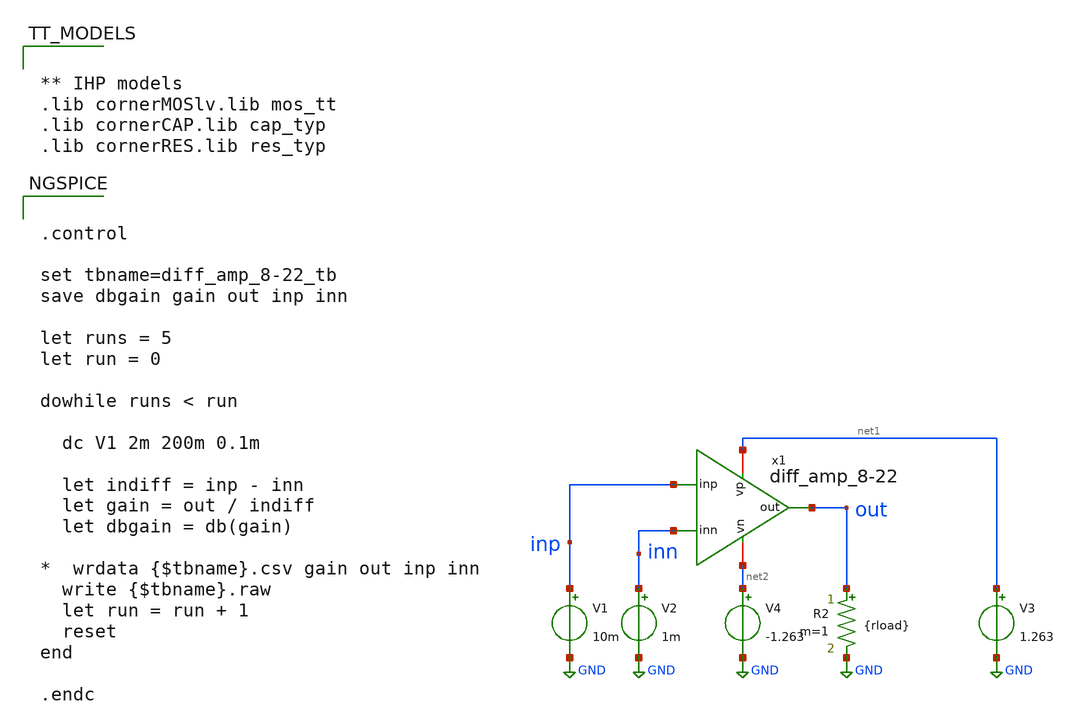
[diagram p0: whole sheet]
** sch_path: TempSensor/design_data/xschem/diff_amp_8-22_tb.sch
**.subckt diff_amp_8-22_tb
V2 inn GND 1m
V1 inp GND 10m
V3 net1 GND 1.263
V4 net2 GND -1.263
x1 net1 out inp inn net2 diff_amp_8-22
R2 out GND {rload} m=1
**** begin user architecture code


** IHP models
.lib cornerMOSlv.lib mos_tt
.lib cornerCAP.lib cap_typ
.lib cornerRES.lib res_typ




.control

set tbname=diff_amp_8-22_tb
save dbgain gain out inp inn

let runs = 5
let run = 0

dowhile runs < run

  dc V1 2m 200m 0.1m

  let indiff = inp - inn
  let gain = out / indiff
  let dbgain = db(gain)

*  wrdata {$tbname}.csv gain out inp inn
  write {$tbname}.raw
  let run = run + 1
  reset
end

.endc


**** end user architecture code
**.ends

* expanding   symbol:  practicing/TempSensor/design_data/xschem/diff_amp_8-22.sym # of pins=5
** sym_path: TempSensor/design_data/xschem/diff_amp_8-22.sym
** sch_path: TempSensor/design_data/xschem/diff_amp_8-22.sch
.subckt diff_amp_8-22 vp out inp inn vn
*.opin out
*.iopin vn
*.iopin vp
*.ipin inp
*.ipin inn
XM5 net18 net1 vp vp sg13_lv_pmos w=10u l=3.33u ng=1 m=1 mm_ok=1
XM30 net15 inn net6 vn sg13_lv_nmos w=10u l=1.5u ng=1 m=5 mm_ok=1
I0 vp net4 5u
XM7 net19 net1 vp vp sg13_lv_pmos w=10u l=3.33u ng=1 m=2 mm_ok=1
XM6 net1 net1 net18 vp sg13_lv_pmos w=10u l=1u ng=1 m=1 mm_ok=1
XM8 net5 net1 net19 vp sg13_lv_pmos w=10u l=.5u ng=1 m=1 mm_ok=1
XM11 net15 net7 vp vp sg13_lv_pmos w=10u l=2.5u ng=1 m=5 mm_ok=1
XM13 net16 net7 vp vp sg13_lv_pmos w=10u l=2.5u ng=1 m=5 mm_ok=1
XM12 net7 net7 net15 vp sg13_lv_pmos w=10u l=1u ng=1 m=5 mm_ok=1
XM14 out net7 net16 vp sg13_lv_pmos w=10u l=1u ng=1 m=5 mm_ok=1
XM21 net12 net12 vp vp sg13_lv_pmos w=10u l=.33u ng=1 m=10 mm_ok=1
XM24 net13 net1 vp vp sg13_lv_pmos w=4u l=5u ng=1 m=1 mm_ok=1
XM22 net11 net11 net12 vp sg13_lv_pmos w=10u l=.33u ng=1 m=10 mm_ok=1
XM29 vp inp net6 vn sg13_lv_nmos w=10u l=1.5u ng=1 m=5 mm_ok=1
XM9 net9 inp net5 net5 sg13_lv_pmos w=10u l=1.5u ng=1 m=10 mm_ok=1
XM10 net8 inn net5 net5 sg13_lv_pmos w=10u l=1.5u ng=1 m=10 mm_ok=1
XM1 net4 net4 net3 vn sg13_lv_nmos w=10u l=2u ng=1 m=1 mm_ok=1
XM2 net3 net4 vn vn sg13_lv_nmos w=5u l=5u ng=1 m=1 mm_ok=1
XM3 net1 net4 net2 vn sg13_lv_nmos w=10u l=2u ng=1 m=1 mm_ok=1
XM4 net2 net4 vn vn sg13_lv_nmos w=5u l=5u ng=1 m=1 mm_ok=1
XM31 net6 net4 net17 vn sg13_lv_nmos w=10u l=1u ng=1 m=1 mm_ok=1
XM32 net17 net4 vn vn sg13_lv_nmos w=10u l=5u ng=1 m=1 mm_ok=1
XM15 net7 net4 net8 vn sg13_lv_nmos w=10u l=1u ng=1 m=5 mm_ok=1
XM16 net8 net4 vn vn sg13_lv_nmos w=10u l=5u ng=1 m=1 mm_ok=1
XM17 net10 net4 net9 vn sg13_lv_nmos w=10u l=1u ng=1 m=5 mm_ok=1
XM18 net9 net4 vn vn sg13_lv_nmos w=10u l=5u ng=1 m=1 mm_ok=1
XM20 net11 net4 vn vn sg13_lv_nmos w=1.5u l=5u ng=1 m=1 mm_ok=1
XM19 net10 net11 out vp sg13_lv_pmos w=10u l=.33u ng=1 m=10 mm_ok=1
XM23 out net13 net10 vn sg13_lv_nmos w=10u l=.5u ng=1 m=5 mm_ok=1
XM25 net13 net13 net14 vn sg13_lv_nmos w=10u l=.5u ng=1 m=5 mm_ok=1
XM26 net14 net14 vn vn sg13_lv_nmos w=10u l=.5u ng=1 m=5 mm_ok=1
XM27 vp out out vp sg13_lv_nmos w=10u l=.33u ng=1 m=10 mm_ok=1
XM28 vn net10 out vn sg13_lv_pmos w=10u l=.5u ng=1 m=5 mm_ok=1
XC1 out out cap_cmim w=3.5e-5 l=3.5e-5 m=1 mm_ok=1
XC2 out net10 cap_cmim w=3.5e-5 l=3.5e-5 m=1 mm_ok=1
.ends

.GLOBAL GND
.end
